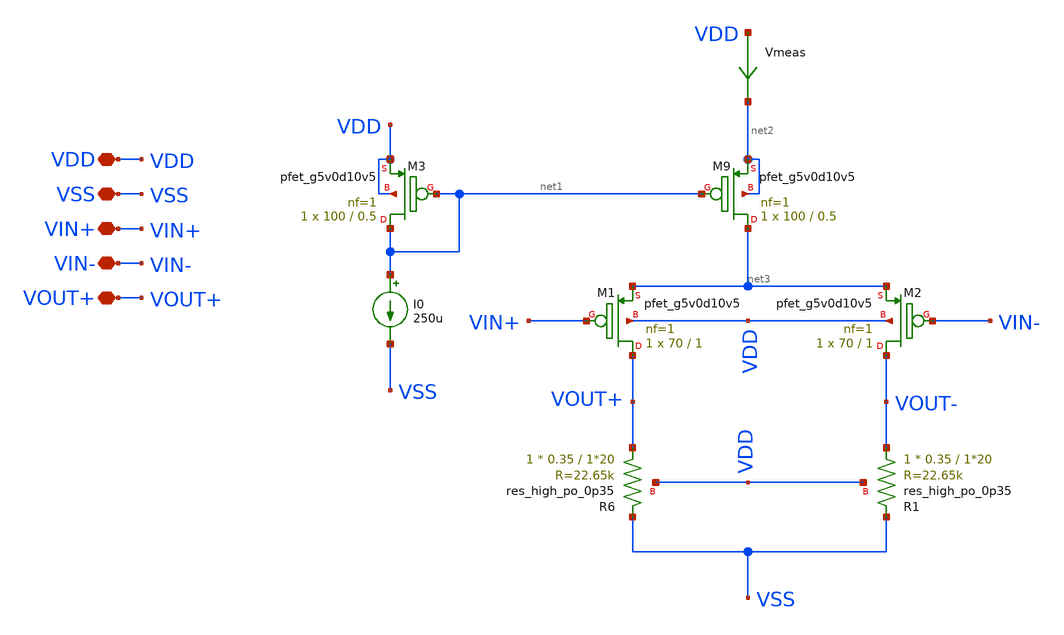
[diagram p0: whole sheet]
** sch_path: amplifiers/differencial_stage_amps/basic_stages/folded_cascode/differential_stage.sch
**.subckt differential_stage VDD VSS VIN+ VIN- VOUT+
*.iopin VDD
*.iopin VSS
*.iopin VIN+
*.iopin VIN-
*.iopin VOUT+
XM9 net3 net1 net2 net2 sky130_fd_pr__pfet_g5v0d10v5 L=0.5 W=100 nf=1 ad='int((1 + 1)/2) * 100 / 1 * 0.29'
+ as='int((1 + 2)/2) * 100 / 1 * 0.29' pd='2*int((1 + 1)/2) * (100 / 1 + 0.29)' ps='2*int((1 + 2)/2) * (100 / 1 + 0.29)'
+ nrd='0.29 / 100 ' nrs='0.29 / 100 ' sa=0 sb=0 sd=0 mult=1 m=1
XM1 VOUT+ VIN+ net3 VDD sky130_fd_pr__pfet_g5v0d10v5 L=1 W=70 nf=1 ad='int((1 + 1)/2) * 70 / 1 * 0.29'
+ as='int((1 + 2)/2) * 70 / 1 * 0.29' pd='2*int((1 + 1)/2) * (70 / 1 + 0.29)' ps='2*int((1 + 2)/2) * (70 / 1 + 0.29)'
+ nrd='0.29 / 70 ' nrs='0.29 / 70 ' sa=0 sb=0 sd=0 mult=1 m=1
XM2 VOUT- VIN- net3 VDD sky130_fd_pr__pfet_g5v0d10v5 L=1 W=70 nf=1 ad='int((1 + 1)/2) * 70 / 1 * 0.29'
+ as='int((1 + 2)/2) * 70 / 1 * 0.29' pd='2*int((1 + 1)/2) * (70 / 1 + 0.29)' ps='2*int((1 + 2)/2) * (70 / 1 + 0.29)'
+ nrd='0.29 / 70 ' nrs='0.29 / 70 ' sa=0 sb=0 sd=0 mult=1 m=1
XR6 VOUT+ VSS VDD sky130_fd_pr__res_high_po_0p35 L=1*20 mult=1 m=1
XR1 VOUT- VSS VDD sky130_fd_pr__res_high_po_0p35 L=1*20 mult=1 m=1
XM3 net1 net1 VDD VDD sky130_fd_pr__pfet_g5v0d10v5 L=0.5 W=100 nf=1 ad='int((1 + 1)/2) * 100 / 1 * 0.29'
+ as='int((1 + 2)/2) * 100 / 1 * 0.29' pd='2*int((1 + 1)/2) * (100 / 1 + 0.29)' ps='2*int((1 + 2)/2) * (100 / 1 + 0.29)'
+ nrd='0.29 / 100 ' nrs='0.29 / 100 ' sa=0 sb=0 sd=0 mult=1 m=1
I0 net1 VSS 250u
Vmeas VDD net2 0
.save i(vmeas)
**.ends
.end
